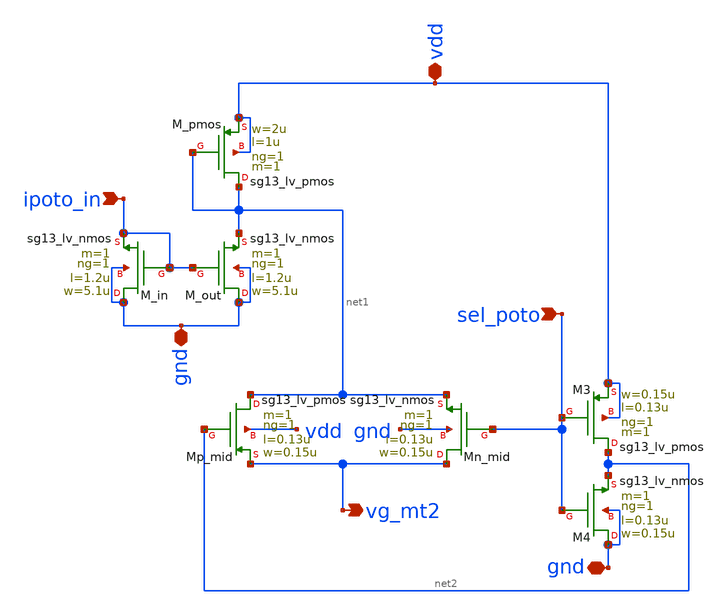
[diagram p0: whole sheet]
** sch_path: Enfoque_B/xschem/celdas/espejo_poto_sel.sch
**.subckt espejo_poto_sel sel_poto ipoto_in gnd vg_mt2 vdd gnd
*.ipin sel_poto
*.ipin ipoto_in
*.iopin gnd
*.opin vg_mt2
*.iopin vdd
*.iopin gnd
XM_out gnd ipoto_in net1 gnd sg13_lv_nmos w=5.1u l=1.2u ng=1 m=1 mm_ok=1
XM_pmos net1 net1 vdd vdd sg13_lv_pmos w=2u l=1u ng=1 m=1 mm_ok=1
XM_in gnd ipoto_in ipoto_in gnd sg13_lv_nmos w=5.1u l=1.2u ng=1 m=1 mm_ok=1
XMn_mid vg_mt2 sel_poto net1 gnd sg13_lv_nmos w=0.15u l=0.13u ng=1 m=1 mm_ok=1
XMp_mid net1 net2 vg_mt2 vdd sg13_lv_pmos w=0.15u l=0.13u ng=1 m=1 mm_ok=1
XM3 net2 sel_poto vdd vdd sg13_lv_pmos w=0.15u l=0.13u ng=1 m=1 mm_ok=1
XM4 gnd sel_poto net2 gnd sg13_lv_nmos w=0.15u l=0.13u ng=1 m=1 mm_ok=1
**.ends
.end
